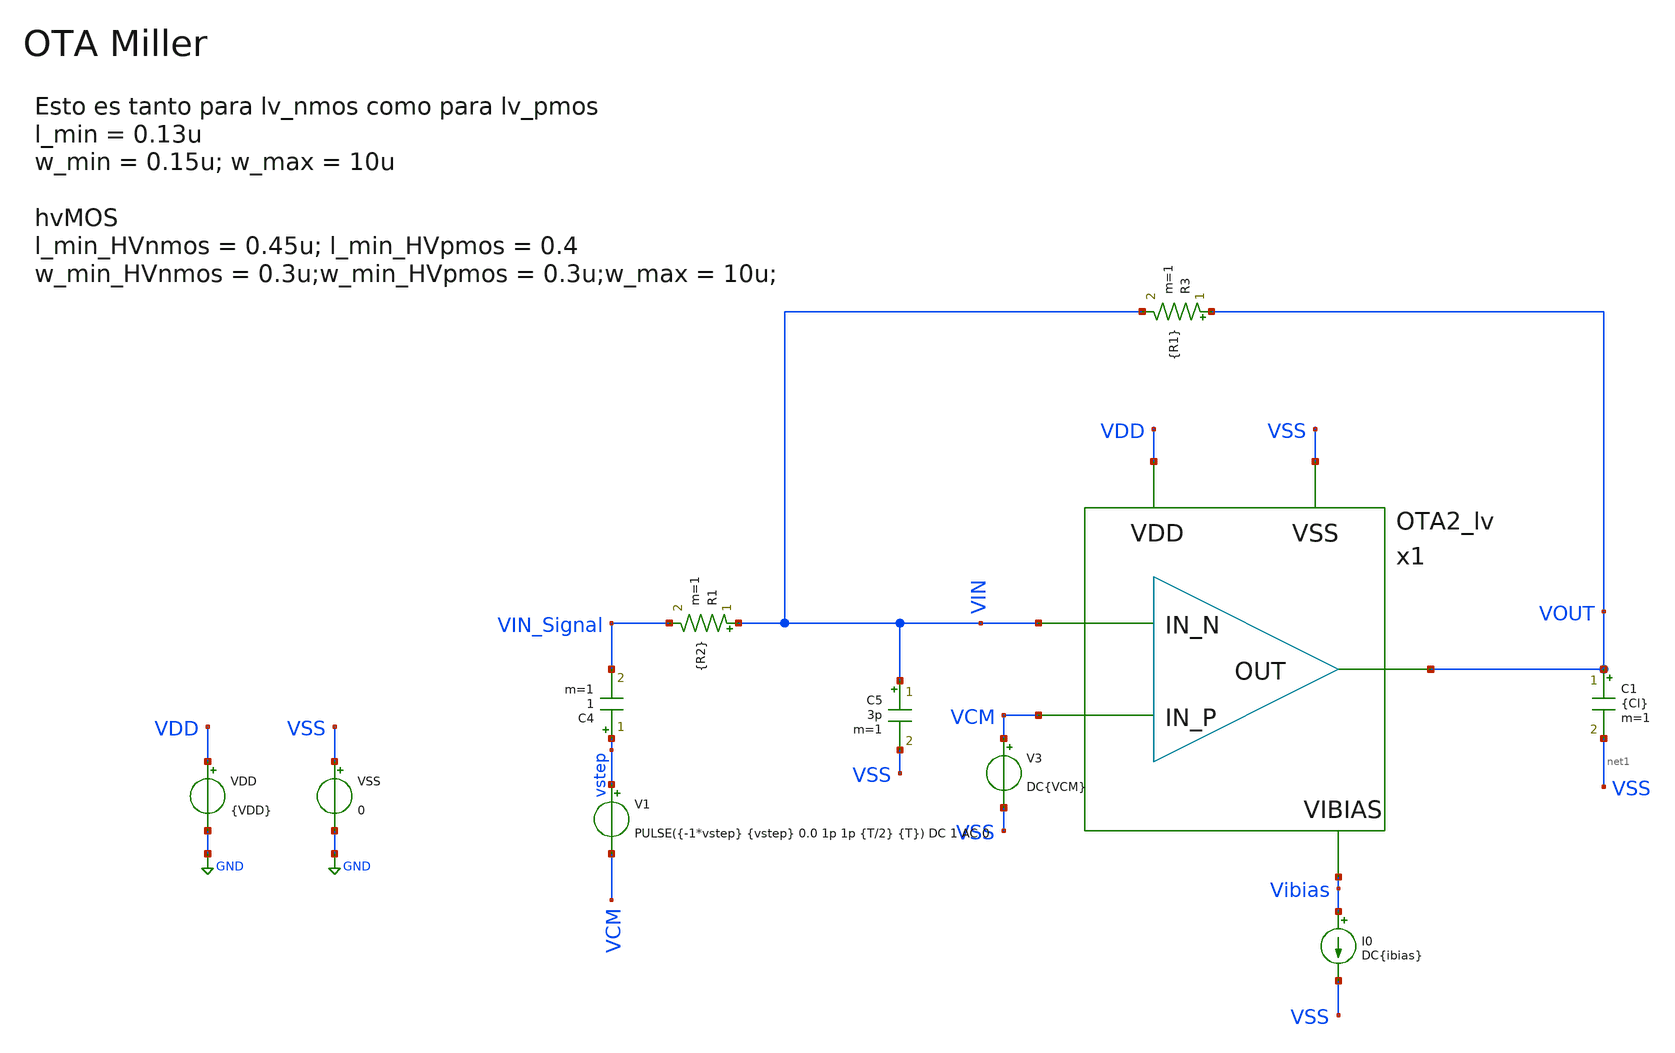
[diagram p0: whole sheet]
** sch_path: xschem/Ayudantias/Ayudantia_2/TB_OTA2_StepResp.sch
**.subckt TB_OTA2_StepResp
VDD VDD GND {VDD}
I0 Vibias VSS DC{ibias}
R3 VOUT VIN {R1} m=1
V3 VCM VSS DC{VCM}
VSS VSS GND 0
C5 VIN VSS 3p m=1
R1 VIN VIN_Signal {R2} m=1
C1 VOUT net1 {Cl} m=1
C4 vstep VIN_Signal 1 m=1
V1 vstep VCM PULSE({-1*vstep} {vstep} 0.0 1p 1p {T/2} {T}) DC 1 AC 0
x1 VIN VCM VOUT VDD VSS Vibias OTA2_lv
**** begin user architecture code


*.param VDD = 3.3
.param VDD = 1.2
.param VCM = 0.6
.param Ibias = 100u
.param Pi = 3.14159265
.param wo = 2*Pi*60Meg
.csparam wo = {wo}

.param VAC = 10m
*.param VAC  = 30m
*.param fin  = 9.765625e5
.param fin  = 1e4
.param T = 1/fin

.param vstep = 10m

.param R1 = 100k
*.param R2 = R1/10
.param R2 = R1/30

*.ic v(Vo) = 0

* OP Parameters & Singals to save
.save all

*.option temp = 125
*.option temp = -40
.option temp = 27





.lib cornerMOShv.lib mos_tt
.lib cornerMOSlv.lib mos_tt
*.lib cornerMOShv.lib mos_ff
*.lib cornerMOSlv.lib mos_ff
*.lib cornerMOShv.lib mos_ss
*.lib cornerMOSlv.lib mos_ss
*.lib cornerMOShv.lib mos_sf
*.lib cornerMOSlv.lib mos_sf
*.lib cornerMOShv.lib mos_fs
*.lib cornerMOSlv.lib mos_fs

.include /opt/pdks/ihp-sg13g2/libs.ref/sg13g2_stdcell/spice/sg13g2_stdcell.spice
.lib $::SG13G2_MODELS/cornerRES.lib res_typ
.lib $::SG13G2_MODELS/cornerCAP.lib cap_typ
*.lib $::SG13G2_MODELS/diodes.lib



.param temp=27

.param m_M8 = 1
.param m_M7 = 1
.param m_M5 = 1
.param w_M8 =0.15u
.param w_M7 =0.15u
.param w_M5 =0.15u
.param l_M875 = 0.13u

.param m_M12 = 1
.param w_M12 =0.15u
.param l_M12 = 0.13u

.param m_M34 = 1
.param w_M34 =0.15u
.param l_M34 = 0.13u

.param m_M6 = 1
.param w_M6 =0.15u
.param l_M6 = 0.13u

.param m_R = 1
.param w_R =0.15u
.param l_R = 0.13u

.param Cc = 0.1p
.param Cl = 5p
.csparam Cl = {Cl}
.csparam Cc = {Cc}






*.param SimTime = 10*T
*.tran 0.01u {SimTime} uic
*.save all v(vsen)
.control

  set color0 = white
  tran 0.1u 100u
  setplot tran1
  *plot v(vsen) v(VOUT)
  plot v(vstep) v(VIN_signal) v(VOUT)
.endc

.end





**** end user architecture code
**.ends

* expanding   symbol:  ../Ayudantia_2/OTA2_lv.sym # of pins=6
** sym_path: ../Ayudantia_2/OTA2_lv.sym
** sch_path: ../Ayudantia_2/OTA2_lv.sch
.subckt OTA2_lv IN_N IN_P OUT VDD VSS Vibias
*.ipin IN_N
*.ipin IN_P
*.ipin Vibias
*.opin OUT
*.iopin VDD
*.iopin VSS
XM1 VB IN_N net1 VA sg13_lv_pmos w={w_M12} l={l_M12} ng=1 m={m_M12} mm_ok=1
XM3 VSS VB VB VSS sg13_lv_nmos w={w_M34} l={l_M34} ng=1 m={m_M34} mm_ok=1
XM2 VC IN_P net2 VA sg13_lv_pmos w={w_M12} l={l_M12} ng=1 m={m_M12} mm_ok=1
XM4 VSS VB net6 VSS sg13_lv_nmos w={w_M34} l={l_M34} ng=1 m={m_M34} mm_ok=1
XM5 net7 Vibias VDD VDD sg13_lv_pmos w={w_M5} l={l_M875} ng=1 m={m_M5} mm_ok=1
XM6 VSS VC net3 VSS sg13_lv_nmos w={w_M6} l={l_M6} ng=1 m={m_M6} mm_ok=1
XM7 net5 Vibias VDD VDD sg13_lv_pmos w={w_M7} l={l_M875} ng=1 m={m_M7} mm_ok=1
XM8 net8 Vibias VDD VDD sg13_lv_pmos w={w_M8} l={l_M875} ng=1 m={m_M8} mm_ok=1
C1 VC net4 {Cc} m=1
Vmeas VA net1 0
.save i(vmeas)
Vmeas1 VC net6 0
.save i(vmeas1)
Vmeas2 VA net2 0
.save i(vmeas2)
Vmeas3 net4 net3 0
.save i(vmeas3)
Vmeas4 net5 net4 0
.save i(vmeas4)
Vmeas5 net7 VA 0
.save i(vmeas5)
Vmeas6 net8 Vibias 0
.save i(vmeas6)
Vmeas7 net4 OUT 0
.save i(vmeas7)
.ends

.GLOBAL GND
.end
